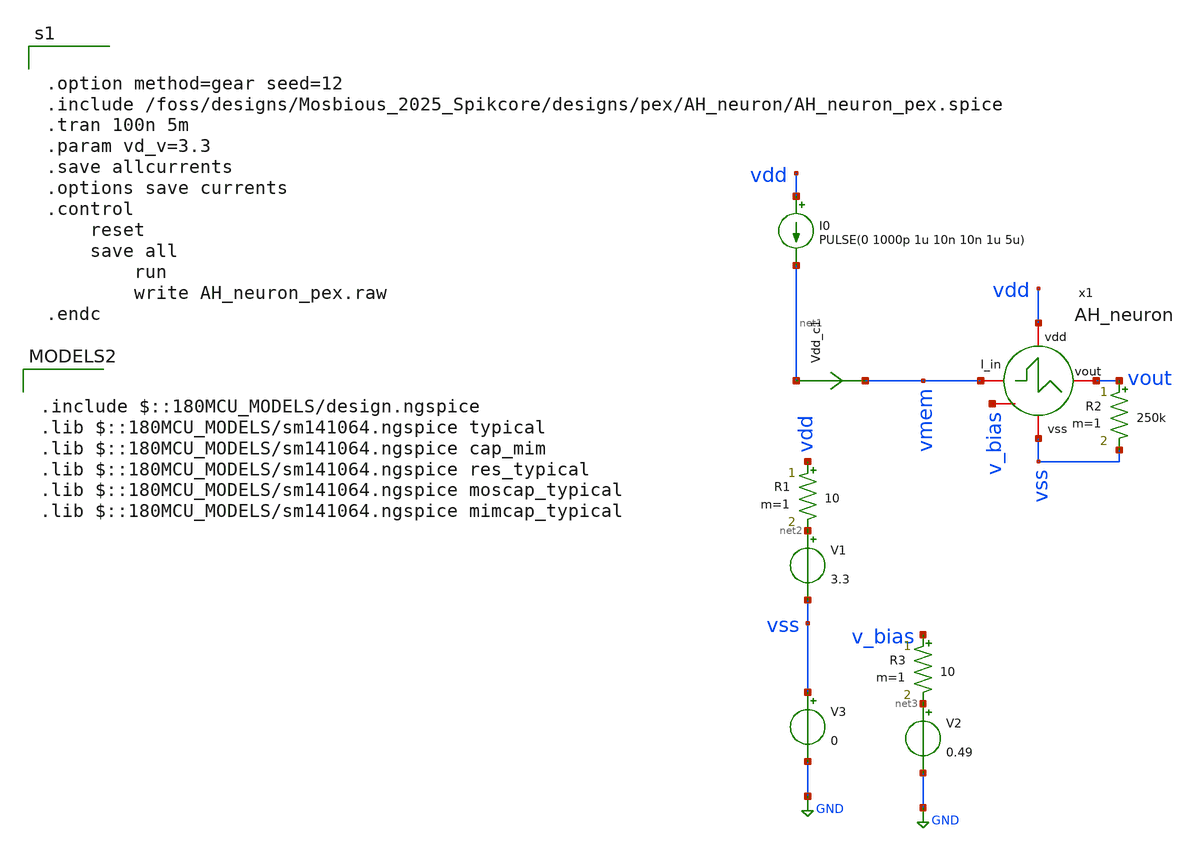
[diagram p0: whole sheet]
** sch_path: designs/pex/AH_neuron/AH_neuron_pex.sch
**.subckt AH_neuron_pex
V1 net2 vss 3.3
I0 vdd net1 PULSE(0 1000p 1u 10n 10n 1u 5u)
R1 vdd net2 10 m=1
R2 vout vss 250k m=1
Vdd_c1 net1 vmem 0
.save i(vdd_c1)
V2 net3 GND 0.49
R3 v_bias net3 10 m=1
V3 vss GND 0
x1 vdd vmem vout vss v_bias AH_neuron
**** begin user architecture code


.option method=gear seed=12
.include /foss/designs/Mosbious_2025_Spikcore/designs/pex/AH_neuron/AH_neuron_pex.spice
.tran 100n 5m
.param vd_v=3.3
.save allcurrents
.options save currents
.control
	reset
	save all
        run
        write AH_neuron_pex.raw
.endc



.include $::180MCU_MODELS/design.ngspice
.lib $::180MCU_MODELS/sm141064.ngspice typical
.lib $::180MCU_MODELS/sm141064.ngspice cap_mim
.lib $::180MCU_MODELS/sm141064.ngspice res_typical
.lib $::180MCU_MODELS/sm141064.ngspice moscap_typical
.lib $::180MCU_MODELS/sm141064.ngspice mimcap_typical

**** end user architecture code
**.ends
.GLOBAL GND
.end
